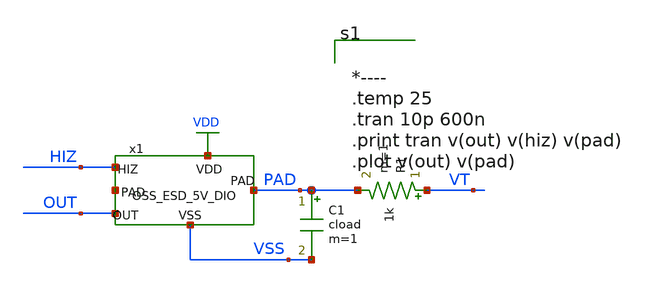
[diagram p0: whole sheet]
** sch_path: schematic/TB/IO_AC.sch
**.subckt IO_AC
x1 VDD PAD VSS HIZ OUT OSS_ESD_5V_DIO
C1 PAD VSS cload m=1
R1 VT PAD 1k m=1
**** begin user architecture code



* ngspice commands
.include '~/Dropbox/91_OpenPDK/TR-1um/libs.tech/spice/models/ip62_models'
.param vdd=5.0
.param vss=0
*----
vdd  vdd 0 dc vdd
vss  vss 0 dc vss
vtt  vt  0 dc 'vdd / 2.0'
.param cload='20p'
.param trf=100p
vout out 0 pwl(0n vss 100n vss '100n+trf' vdd  200n vdd  '200n+trf' vss R)
vhiz hiz 0 pwl(0n vss 500n vss '500n+trf' vdd 1000n vdd '1000n+trf' vss R)



**** end user architecture code
**.ends
.GLOBAL VDD
**** begin user architecture code


*----
.temp 25
.tran 10p 600n
.print tran v(out) v(hiz) v(pad)
.plot v(out) v(pad)


**** end user architecture code
.end
